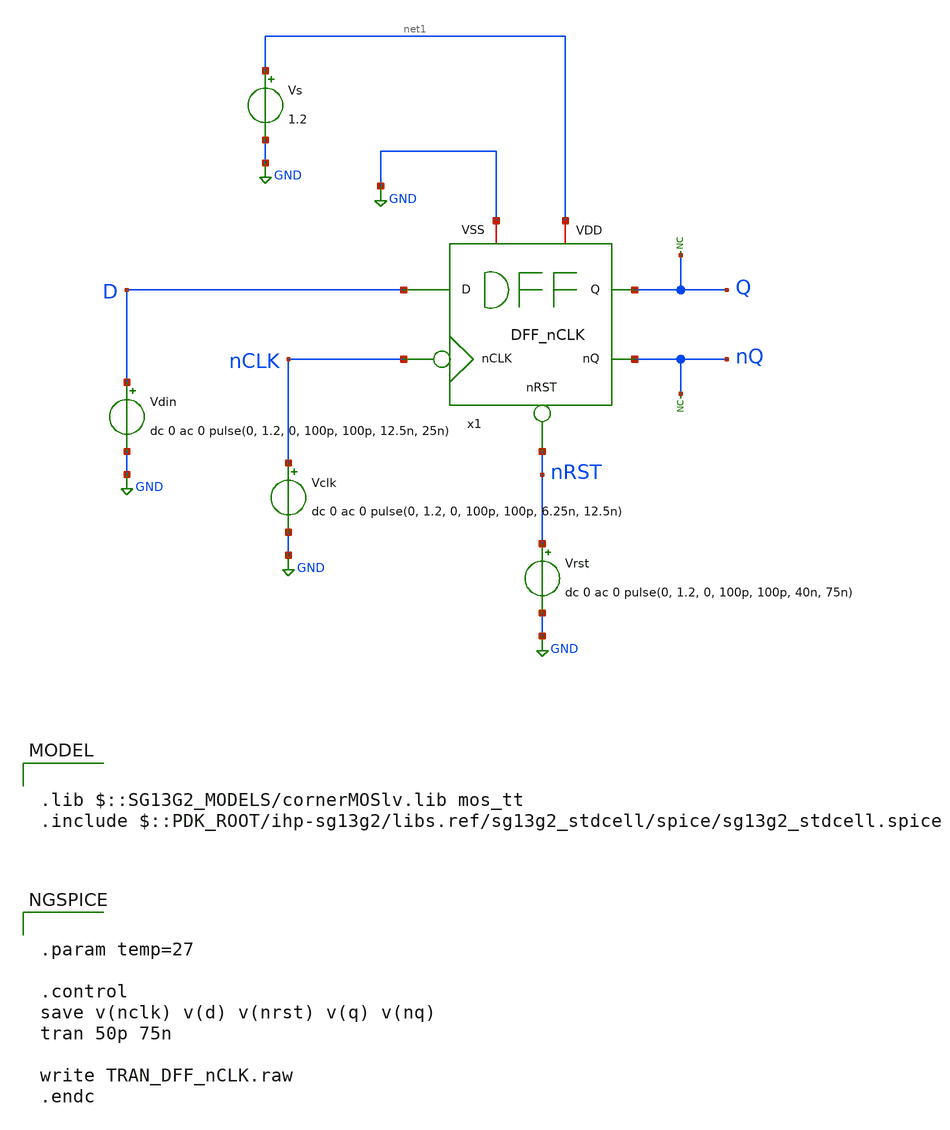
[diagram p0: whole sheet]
** sch_path: 30_MHz_Fractional_N_PLL/design_data/xschem/DFF_nCLK_TB.sch

.lib $::SG13G2_MODELS/cornerMOSlv.lib mos_tt
.include $::PDK_ROOT/ihp-sg13g2/libs.ref/sg13g2_stdcell/spice/sg13g2_stdcell.spice

**.subckt DFF_nCLK_TB
Vdin D GND dc 0 ac 0 pulse(0, 1.2, 0, 100p, 100p, 12.5n, 25n)
Vclk nCLK GND dc 0 ac 0 pulse(0, 1.2, 0, 100p, 100p, 6.25n, 12.5n)
Vrst nRST GND dc 0 ac 0 pulse(0, 1.2, 0, 100p, 100p, 40n, 75n)
* noconn nQ
* noconn Q
x1 nCLK Q D nQ nRST net1 GND DFF_nCLK
Vs net1 GND 1.2
**** begin user architecture code


.param temp=27

.control
save v(nclk) v(d) v(nrst) v(q) v(nq)
tran 50p 75n

write TRAN_DFF_nCLK.raw
.endc


**** end user architecture code
**.ends

* expanding   symbol:  DFF_nCLK.sym # of pins=7
** sym_path: 30_MHz_Fractional_N_PLL/design_data/xschem/DFF_nCLK.sym
** sch_path: 30_MHz_Fractional_N_PLL/design_data/xschem/DFF_nCLK.sch
.subckt DFF_nCLK nCLK Q D nQ nRST VDD VSS
*.ipin nCLK
*.ipin D
*.ipin nRST
*.opin Q
*.opin nQ
*.iopin VSS
*.iopin VDD
x1 Q nQ net1 D nRST VDD VSS sg13g2_dfrbp_1
x2 net1 nCLK VDD VSS sg13g2_inv_1
.ends


* expanding   symbol:  sg13g2_stdcells/sg13g2_dfrbp_1.sym # of pins=5
** sym_path: sg13g2_stdcells/sg13g2_dfrbp_1.sym
** sch_path: sg13g2_stdcells/sg13g2_dfrbp_1.sch
.subckt sg13g2_dfrbp_1 Q Q_N CLK D RESET_B VDD VSS
*.ipin D
*.ipin RESET_B
*.ipin CLK
*.opin Q
*.opin Q_N
*.iopin VDD
*.iopin VSS
XM1 Db D net10 VSS sg13_lv_nmos w=420.00n l=130.00n ng=1 m=1 mm_ok=1
XM2 net10 RESET_B VSS VSS sg13_lv_nmos w=420.00n l=130.00n ng=1 m=1 mm_ok=1
XM3 net1 clkneg net9 VSS sg13_lv_nmos w=420.00n l=130.00n ng=1 m=1 mm_ok=1
XM4 net9 net1 VSS VSS sg13_lv_nmos w=420.00n l=130.00n ng=1 m=1 mm_ok=1
XM5 net1 net1 net5 VSS sg13_lv_nmos w=420.00n l=130.00n ng=1 m=1 mm_ok=1
XM6 net5 RESET_B VSS VSS sg13_lv_nmos w=420.00n l=130.00n ng=1 m=1 mm_ok=1
XM7 Q_N net1 VSS VSS sg13_lv_nmos w=740.00n l=130.00n ng=1 m=1 mm_ok=1
XM8 net2 net1 VSS VSS sg13_lv_nmos w=740.00n l=130.00n ng=1 m=1 mm_ok=1
XM9 Q net2 VSS VSS sg13_lv_nmos w=740.00n l=130.00n ng=1 m=1 mm_ok=1
XM10 clkneg CLK VSS VSS sg13_lv_nmos w=740.00n l=130.00n ng=1 m=1 mm_ok=1
XM11 clkpos clkneg VSS VSS sg13_lv_nmos w=740.00n l=130.00n ng=1 m=1 mm_ok=1
XM12 Db clkneg net3 VSS sg13_lv_nmos w=420.00n l=130.00n ng=1 m=1 mm_ok=1
XM13 net3 clkpos net8 VSS sg13_lv_nmos w=420.00n l=130.00n ng=1 m=1 mm_ok=1
XM14 net8 net3 net4 VSS sg13_lv_nmos w=420.00n l=130.00n ng=1 m=1 mm_ok=1
XM15 net4 RESET_B VSS VSS sg13_lv_nmos w=420.00n l=130.00n ng=1 m=1 mm_ok=1
XM16 net3 net3 VSS VSS sg13_lv_nmos w=740.00n l=130.00n ng=1 m=1 mm_ok=1
XM17 net3 clkpos net1 VSS sg13_lv_nmos w=740.00n l=130.00n ng=1 m=1 mm_ok=1
XM18 Db RESET_B VDD VDD sg13_lv_pmos w=420.00n l=130.00n ng=1 m=1 mm_ok=1
XM19 Db D VDD VDD sg13_lv_pmos w=420.00n l=130.00n ng=1 m=1 mm_ok=1
XM20 net7 net1 VDD VDD sg13_lv_pmos w=420.00n l=130.00n ng=1 m=1 mm_ok=1
XM21 net1 clkpos net7 VDD sg13_lv_pmos w=420.00n l=130.00n ng=1 m=1 mm_ok=1
XM22 net1 net1 VDD VDD sg13_lv_pmos w=420.00n l=130.00n ng=1 m=1 mm_ok=1
XM23 net1 RESET_B VDD VDD sg13_lv_pmos w=420.00n l=130.00n ng=1 m=1 mm_ok=1
XM24 Q_N net1 VDD VDD sg13_lv_pmos w=1.12u l=130.00n ng=1 m=1 mm_ok=1
XM25 net2 net1 VDD VDD sg13_lv_pmos w=1.12u l=130.00n ng=1 m=1 mm_ok=1
XM26 Q net2 VDD VDD sg13_lv_pmos w=1.12u l=130.00n ng=1 m=1 mm_ok=1
XM27 clkneg CLK VDD VDD sg13_lv_pmos w=1.12u l=130.00n ng=1 m=1 mm_ok=1
XM28 clkpos clkneg VDD VDD sg13_lv_pmos w=1.12u l=130.00n ng=1 m=1 mm_ok=1
XM29 Db clkpos net3 VDD sg13_lv_pmos w=420.00n l=130.00n ng=1 m=1 mm_ok=1
XM30 net6 net3 VDD VDD sg13_lv_pmos w=420.00n l=130.00n ng=1 m=1 mm_ok=1
XM31 net3 clkneg net6 VDD sg13_lv_pmos w=420.00n l=130.00n ng=1 m=1 mm_ok=1
XM32 net3 RESET_B VDD VDD sg13_lv_pmos w=420.00n l=130.00n ng=1 m=1 mm_ok=1
XM33 net3 net3 VDD VDD sg13_lv_pmos w=1.000u l=130.00n ng=1 m=1 mm_ok=1
XM34 net3 clkneg net1 VDD sg13_lv_pmos w=1.000u l=130.00n ng=1 m=1 mm_ok=1
.ends


* expanding   symbol:  sg13g2_stdcells/sg13g2_inv_1.sym # of pins=2
** sym_path: sg13g2_stdcells/sg13g2_inv_1.sym
** sch_path: sg13g2_stdcells/sg13g2_inv_1.sch
.subckt sg13g2_inv_1 Y A VDD VSS
*.opin Y
*.ipin A
*.iopin VDD
*.iopin VSS
XM1 Y A VSS VSS sg13_lv_nmos w=740.00n l=130.00n ng=1 m=1 mm_ok=1
XM2 Y A VDD VDD sg13_lv_pmos w=1.12u l=130.00n ng=1 m=1 mm_ok=1
.ends

.GLOBAL GND
.end
